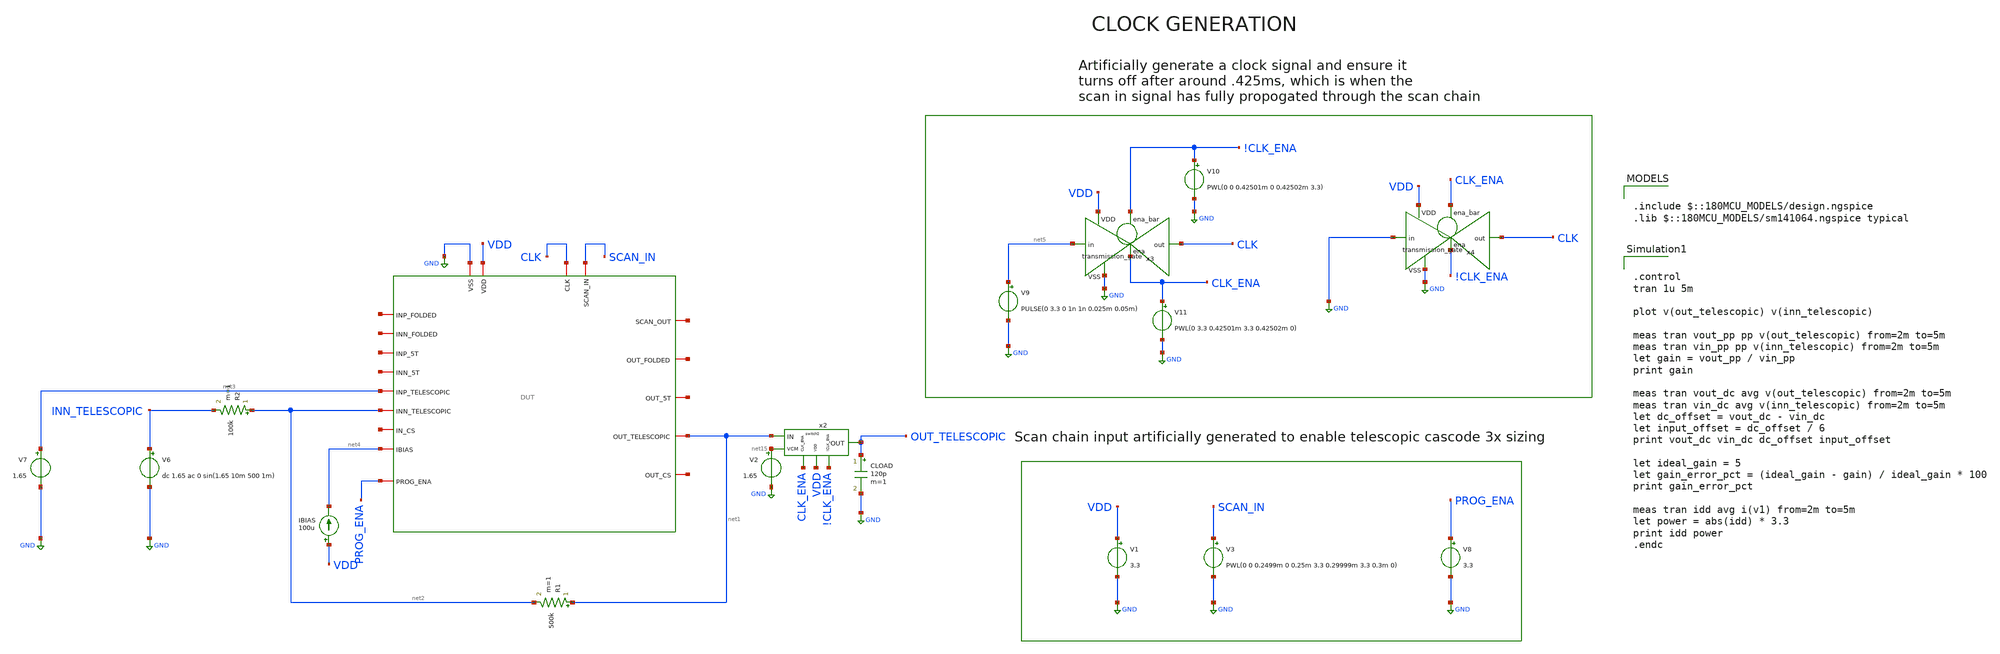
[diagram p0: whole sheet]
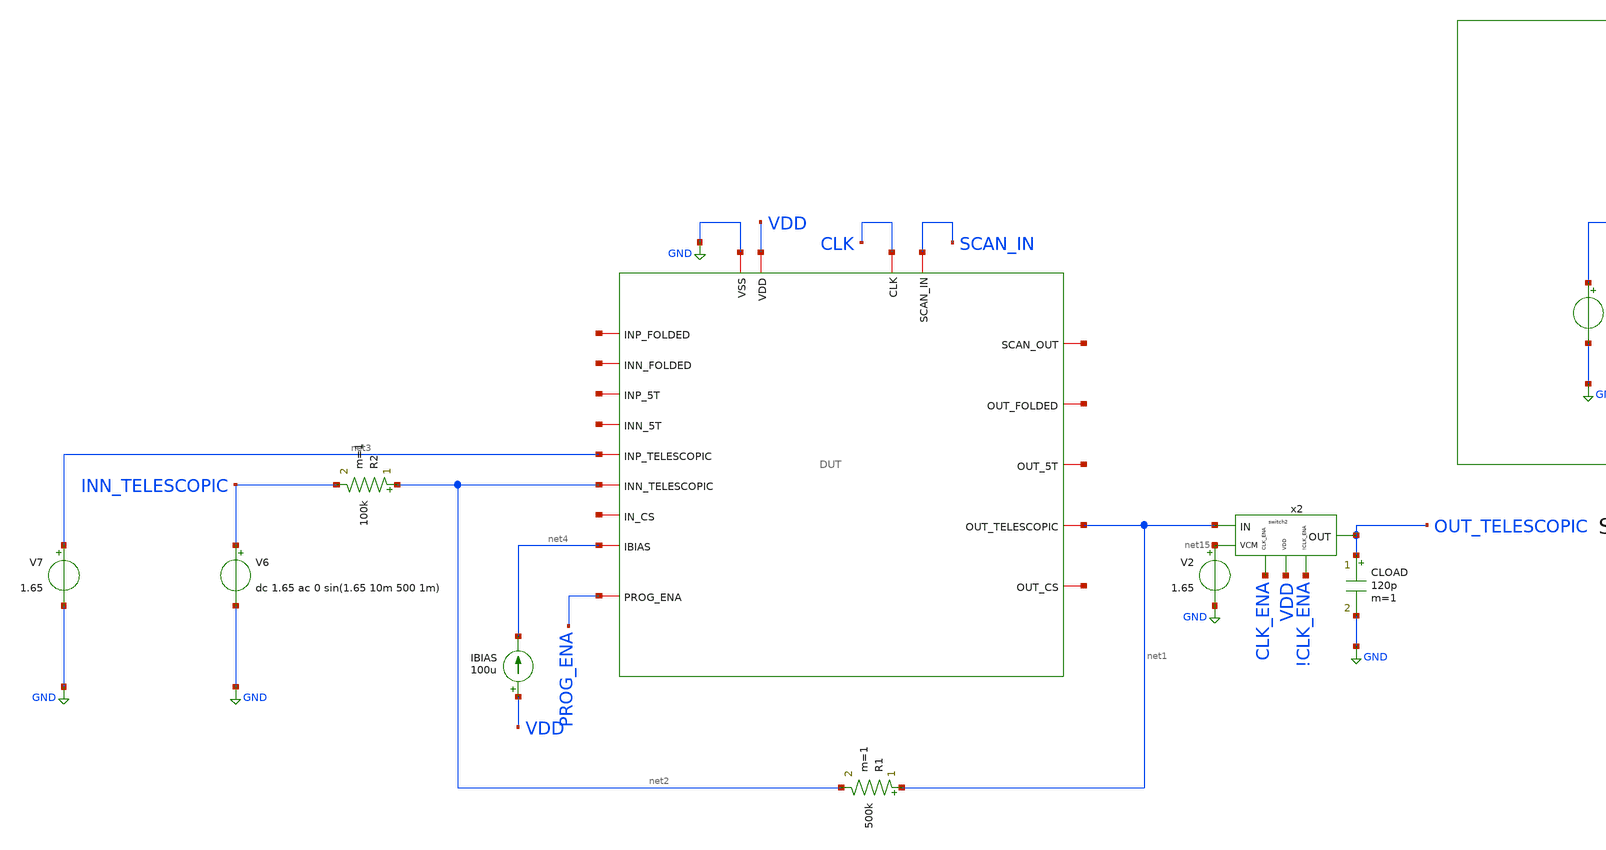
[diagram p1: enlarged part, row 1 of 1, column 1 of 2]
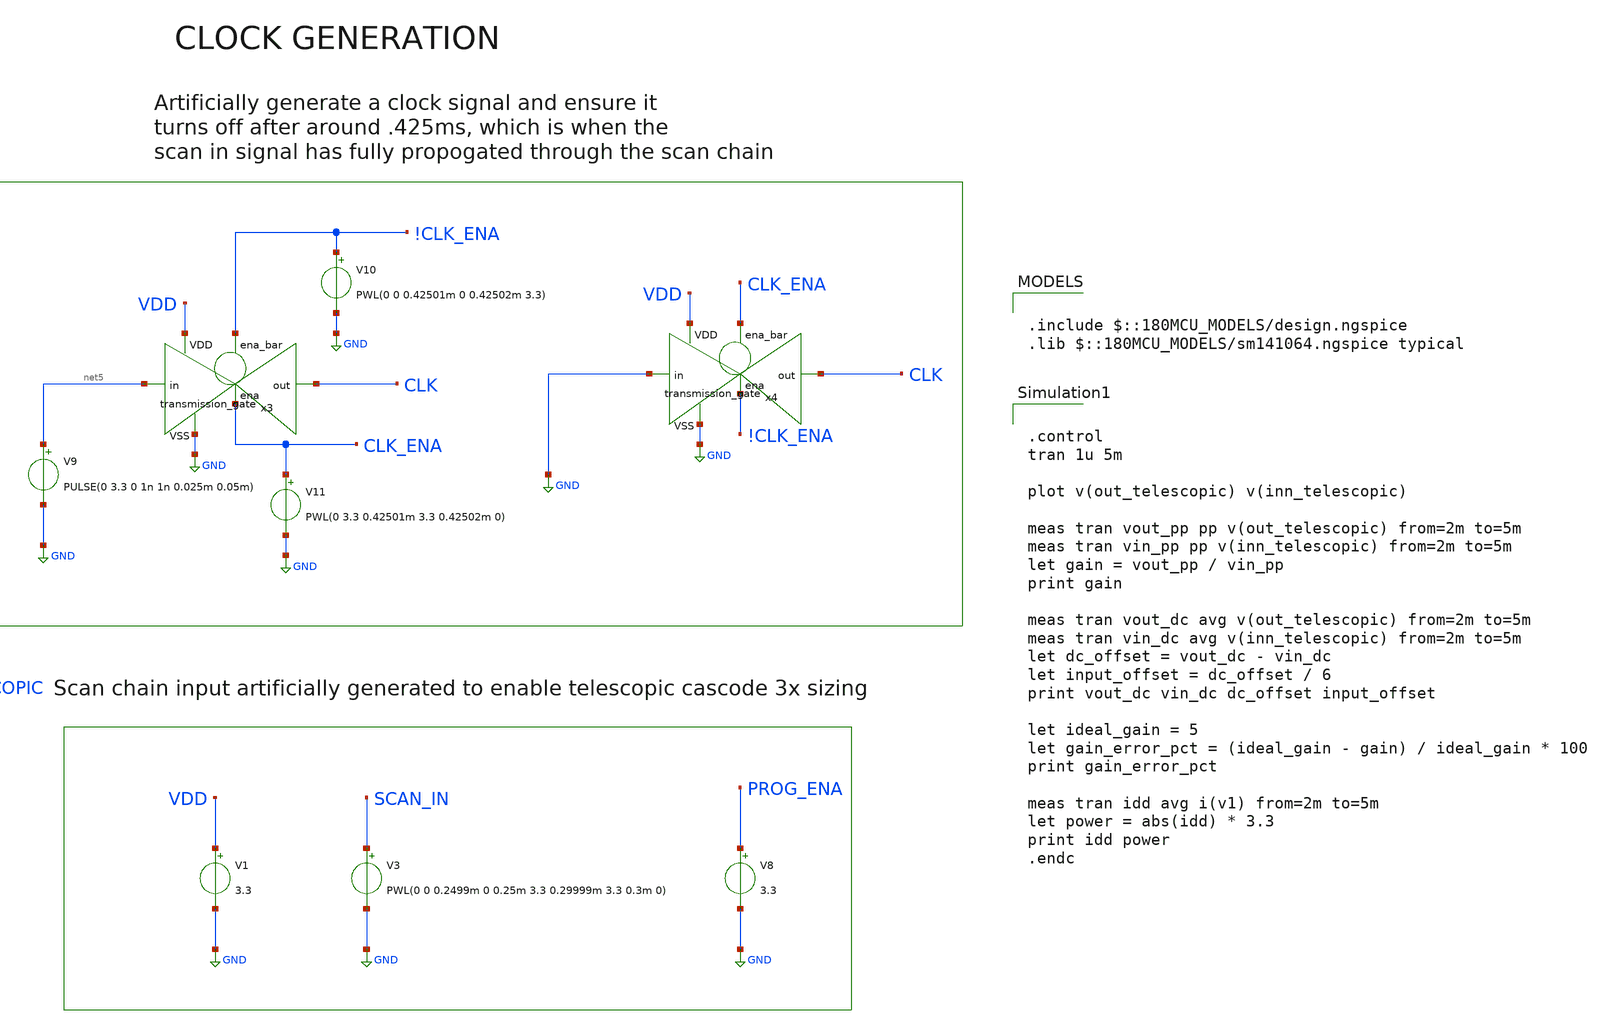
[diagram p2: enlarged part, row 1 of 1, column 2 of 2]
** sch_path: designs/libs/verification/ota_5t/3x_sizing/tele_3x_inverting_clean_noCap.sch
**.subckt tele_3x_inverting_clean_noCap
x1 CLK net6 SCAN_IN GND VDD net7 net8 net9 net4 net10 net11 net12 net3 net1 net13 net14 net2
+ PROG_ENA DUT
CLOAD OUT_TELESCOPIC GND 120p m=1
R1 net1 net2 500k m=1
R2 net2 INN_TELESCOPIC 100k m=1
V6 INN_TELESCOPIC GND dc 1.65 ac 0 sin(1.65 10m 500 1m)
V7 net3 GND 1.65
IBIAS VDD net4 100u
V3 SCAN_IN GND PWL(0 0 0.2499m 0 0.25m 3.3 0.29999m 3.3 0.3m 0)
V1 VDD GND 3.3
V8 PROG_ENA GND 3.3
V9 net5 GND PULSE(0 3.3 0 1n 1n 0.025m 0.05m)
x3 !CLK_ENA VDD CLK net5 GND CLK_ENA transmission_gate
V10 !CLK_ENA GND PWL(0 0 0.42501m 0 0.42502m 3.3)
V11 CLK_ENA GND PWL(0 3.3 0.42501m 3.3 0.42502m 0)
x4 CLK_ENA VDD CLK GND GND !CLK_ENA transmission_gate
V2 net15 GND 1.65
x2 CLK_ENA VDD !CLK_ENA net1 OUT_TELESCOPIC net15 switch2
**** begin user architecture code

.include $::180MCU_MODELS/design.ngspice
.lib $::180MCU_MODELS/sm141064.ngspice typical



.control
tran 1u 5m

plot v(out_telescopic) v(inn_telescopic)

meas tran vout_pp pp v(out_telescopic) from=2m to=5m
meas tran vin_pp pp v(inn_telescopic) from=2m to=5m
let gain = vout_pp / vin_pp
print gain

meas tran vout_dc avg v(out_telescopic) from=2m to=5m
meas tran vin_dc avg v(inn_telescopic) from=2m to=5m
let dc_offset = vout_dc - vin_dc
let input_offset = dc_offset / 6
print vout_dc vin_dc dc_offset input_offset

let ideal_gain = 5
let gain_error_pct = (ideal_gain - gain) / ideal_gain * 100
print gain_error_pct

meas tran idd avg i(v1) from=2m to=5m
let power = abs(idd) * 3.3
print idd power
.endc


**** end user architecture code
**.ends
.GLOBAL GND
.end
